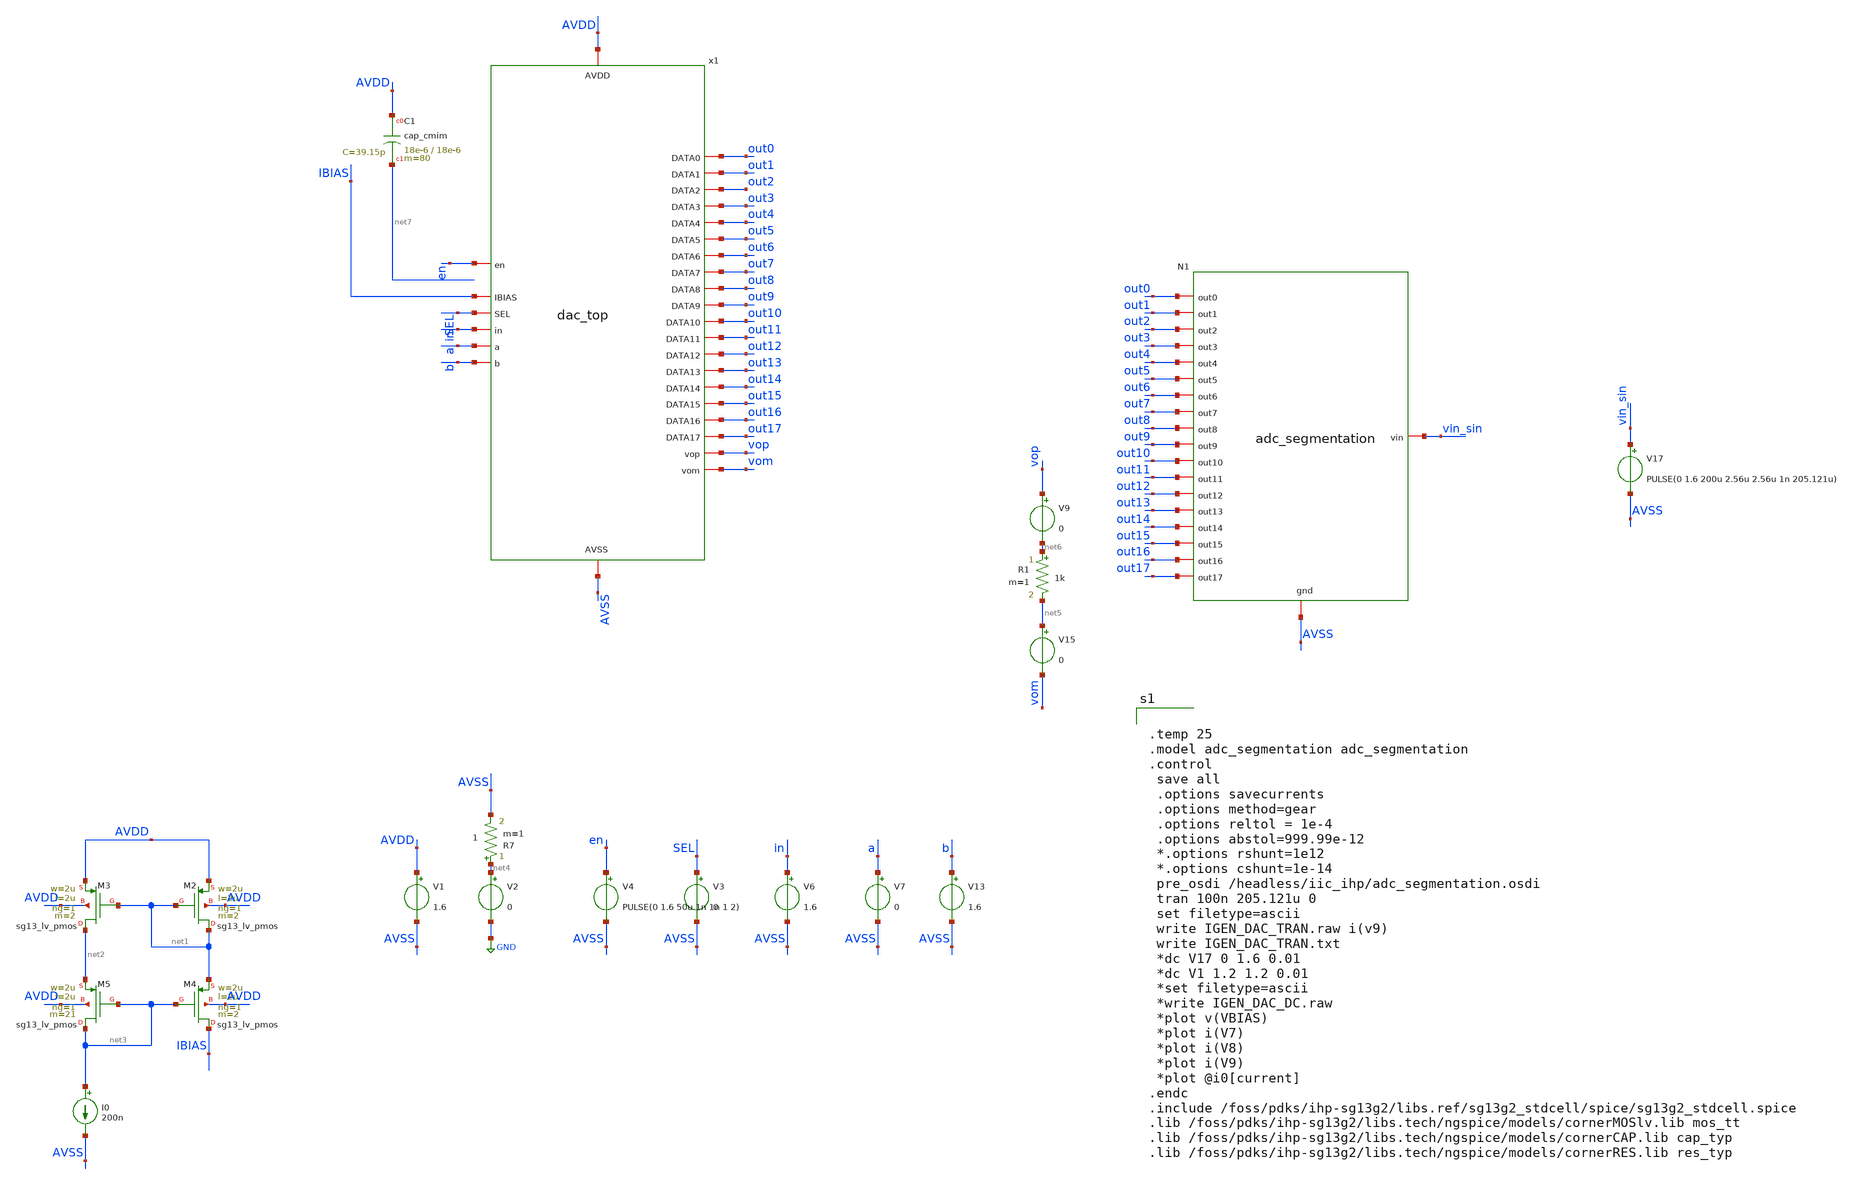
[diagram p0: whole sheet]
** sch_path: current_generator/analog/DAC/schematics/test.sch
**.subckt test
I0 net3 AVSS 200n
V1 AVDD AVSS 1.6
V2 net4 GND 0
V3 SEL AVSS 0
V6 in AVSS 1.6
XM2 net1 net1 AVDD AVDD sg13_lv_pmos w=2u l=2u ng=1 m=2 mm_ok=1
XM3 net2 net1 AVDD AVDD sg13_lv_pmos w=2u l=2u ng=1 m=2 mm_ok=1
XM4 IBIAS net3 net1 AVDD sg13_lv_pmos w=2u l=2u ng=1 m=2 mm_ok=1
XM5 net3 net3 net2 AVDD sg13_lv_pmos w=2u l=2u ng=1 m=21 mm_ok=1
N1 vin_sin AVSS out0 out10 out11 out1 out2 out12 out3 out13 out4 out14 out5 out15 out6 out16 out17
+ out7 out8 out9 adc_segmentation
V7 a AVSS 0
V13 b AVSS 1.6
V17 vin_sin AVSS PULSE(0 1.6 200u 2.56u 2.56u 1n 205.121u)
V4 en AVSS PULSE(0 1.6 50u 1n 1n 1 2)
R7 net4 AVSS 1 m=1
V9 vop net6 0
V15 net5 vom 0
R1 net6 net5 1k m=1
XC1 AVDD net7 cap_cmim w=18e-6 l=18e-6 m=80 mm_ok=1
x1 vom AVDD en IBIAS SEL in a b vop out3 out4 out5 out6 out7 out0 out8 out1 out9 out2 out10 out11
+ out12 out13 out14 out15 out16 out17 AVSS dac_top
**** begin user architecture code


.temp 25
.model adc_segmentation adc_segmentation
.control
 save all
 .options savecurrents
 .options method=gear
 .options reltol = 1e-4
 .options abstol=999.99e-12
 *.options rshunt=1e12
 *.options cshunt=1e-14
 pre_osdi /headless/iic_ihp/adc_segmentation.osdi
 tran 100n 205.121u 0
 set filetype=ascii
 write IGEN_DAC_TRAN.raw i(v9)
 write IGEN_DAC_TRAN.txt
 *dc V17 0 1.6 0.01
 *dc V1 1.2 1.2 0.01
 *set filetype=ascii
 *write IGEN_DAC_DC.raw
 *plot v(VBIAS)
 *plot i(V7)
 *plot i(V8)
 *plot i(V9)
 *plot @i0[current]
.endc
.include /foss/pdks/ihp-sg13g2/libs.ref/sg13g2_stdcell/spice/sg13g2_stdcell.spice
.lib /foss/pdks/ihp-sg13g2/libs.tech/ngspice/models/cornerMOSlv.lib mos_tt
.lib /foss/pdks/ihp-sg13g2/libs.tech/ngspice/models/cornerCAP.lib cap_typ
.lib /foss/pdks/ihp-sg13g2/libs.tech/ngspice/models/cornerRES.lib res_typ


**** end user architecture code
**.ends
.GLOBAL GND
.end
